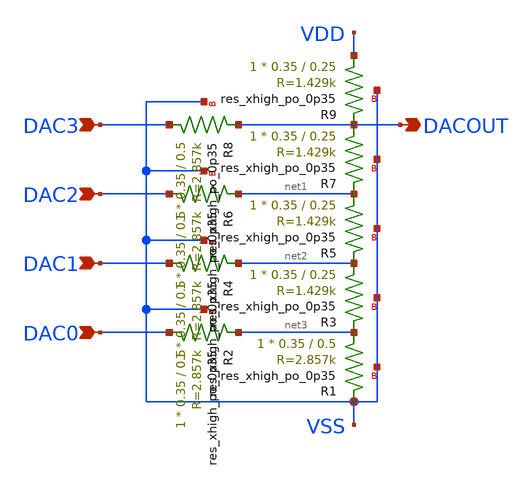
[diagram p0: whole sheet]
** sch_path: tt_um_wulf_8bit_vco/xschem/lib/dac_4bit.sch
**.subckt dac_4bit DAC3 DAC2 DAC1 DAC0 DACOUT
*.ipin DAC3
*.ipin DAC2
*.ipin DAC1
*.ipin DAC0
*.opin DACOUT
XR1 net3 VSS VSS sky130_fd_pr__res_xhigh_po_0p35 L=0.5 mult=1 m=1
XR2 DAC0 net3 VSS sky130_fd_pr__res_xhigh_po_0p35 L=0.5 mult=1 m=1
XR3 net2 net3 VSS sky130_fd_pr__res_xhigh_po_0p35 L=0.25 mult=1 m=1
XR4 DAC1 net2 VSS sky130_fd_pr__res_xhigh_po_0p35 L=0.5 mult=1 m=1
XR5 net1 net2 VSS sky130_fd_pr__res_xhigh_po_0p35 L=0.25 mult=1 m=1
XR6 DAC2 net1 VSS sky130_fd_pr__res_xhigh_po_0p35 L=0.5 mult=1 m=1
XR7 DACOUT net1 VSS sky130_fd_pr__res_xhigh_po_0p35 L=0.25 mult=1 m=1
XR8 DAC3 DACOUT VSS sky130_fd_pr__res_xhigh_po_0p35 L=0.5 mult=1 m=1
XR9 VDD DACOUT VSS sky130_fd_pr__res_xhigh_po_0p35 L=0.25 mult=1 m=1
**.ends
.end
